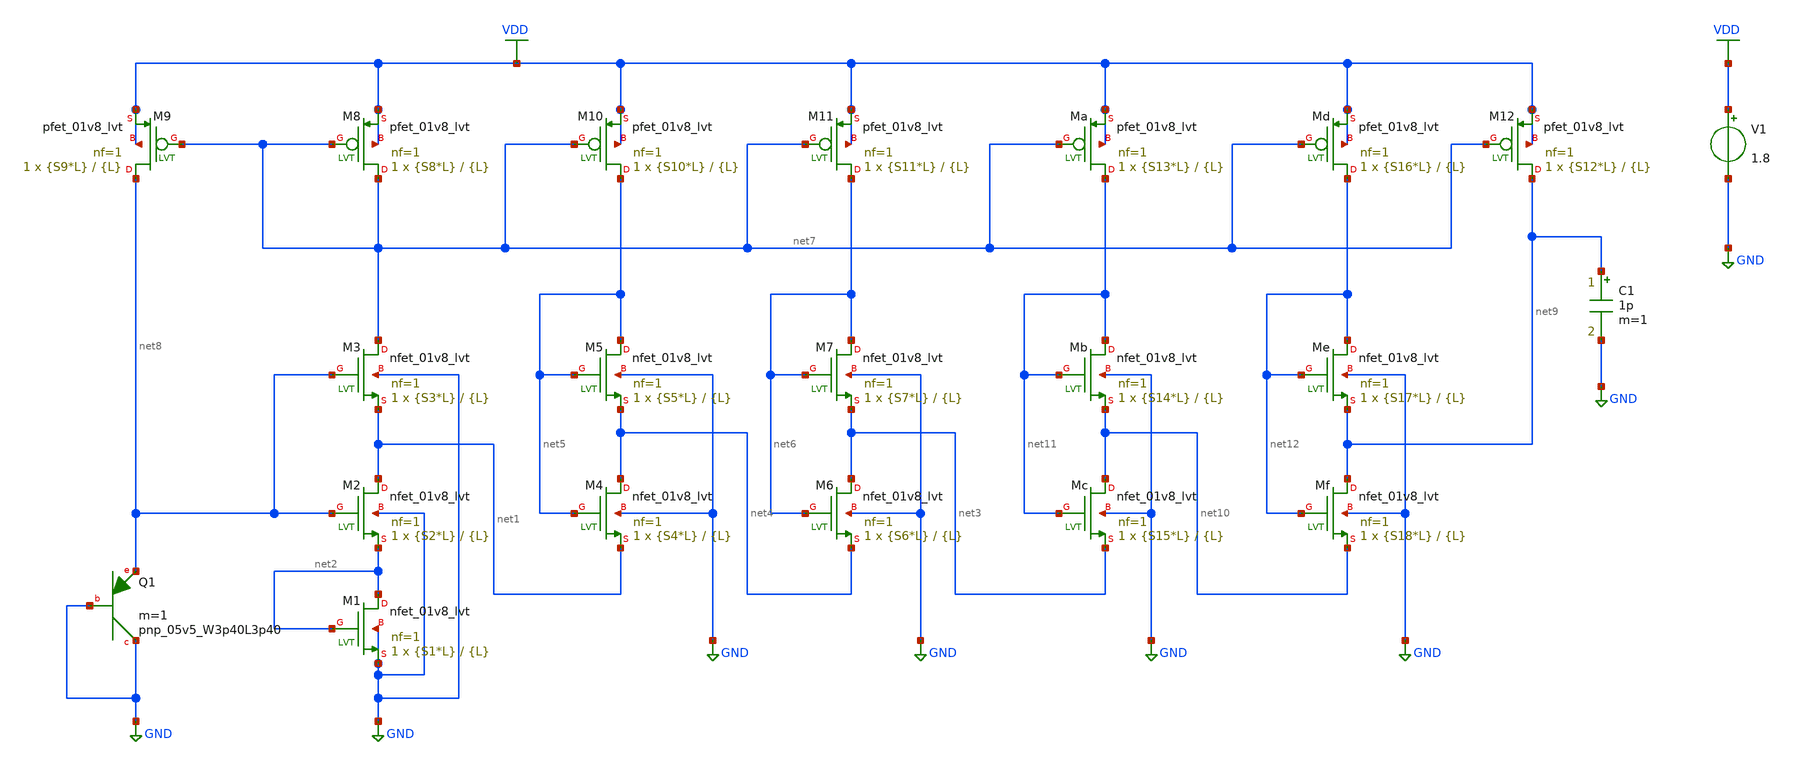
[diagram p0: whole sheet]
** sch_path: Design/Schematic/BGR_SKY130_v3.sch
**.subckt BGR_SKY130_v3
XM1 net2 net2 GND GND sky130_fd_pr__nfet_01v8_lvt L={L} W={S1*L} nf=1 ad='int((nf+1)/2) * W/nf * 0.29'
+ as='int((nf+2)/2) * W/nf * 0.29' pd='2*int((nf+1)/2) * (W/nf + 0.29)' ps='2*int((nf+2)/2) * (W/nf + 0.29)'
+ nrd='0.29 / W' nrs='0.29 / W' sa=0 sb=0 sd=0 mult=1 m=1
XM2 net1 net8 net2 GND sky130_fd_pr__nfet_01v8_lvt L={L} W={S2*L} nf=1 ad='int((nf+1)/2) * W/nf * 0.29'
+ as='int((nf+2)/2) * W/nf * 0.29' pd='2*int((nf+1)/2) * (W/nf + 0.29)' ps='2*int((nf+2)/2) * (W/nf + 0.29)'
+ nrd='0.29 / W' nrs='0.29 / W' sa=0 sb=0 sd=0 mult=1 m=1
XM3 net7 net8 net1 GND sky130_fd_pr__nfet_01v8_lvt L={L} W={S3*L} nf=1 ad='int((nf+1)/2) * W/nf * 0.29'
+ as='int((nf+2)/2) * W/nf * 0.29' pd='2*int((nf+1)/2) * (W/nf + 0.29)' ps='2*int((nf+2)/2) * (W/nf + 0.29)'
+ nrd='0.29 / W' nrs='0.29 / W' sa=0 sb=0 sd=0 mult=1 m=1
XM4 net4 net5 net1 GND sky130_fd_pr__nfet_01v8_lvt L={L} W={S4*L} nf=1 ad='int((nf+1)/2) * W/nf * 0.29'
+ as='int((nf+2)/2) * W/nf * 0.29' pd='2*int((nf+1)/2) * (W/nf + 0.29)' ps='2*int((nf+2)/2) * (W/nf + 0.29)'
+ nrd='0.29 / W' nrs='0.29 / W' sa=0 sb=0 sd=0 mult=1 m=1
XM5 net5 net5 net4 GND sky130_fd_pr__nfet_01v8_lvt L={L} W={S5*L} nf=1 ad='int((nf+1)/2) * W/nf * 0.29'
+ as='int((nf+2)/2) * W/nf * 0.29' pd='2*int((nf+1)/2) * (W/nf + 0.29)' ps='2*int((nf+2)/2) * (W/nf + 0.29)'
+ nrd='0.29 / W' nrs='0.29 / W' sa=0 sb=0 sd=0 mult=1 m=1
XM6 net3 net6 net4 GND sky130_fd_pr__nfet_01v8_lvt L={L} W={S6*L} nf=1 ad='int((nf+1)/2) * W/nf * 0.29'
+ as='int((nf+2)/2) * W/nf * 0.29' pd='2*int((nf+1)/2) * (W/nf + 0.29)' ps='2*int((nf+2)/2) * (W/nf + 0.29)'
+ nrd='0.29 / W' nrs='0.29 / W' sa=0 sb=0 sd=0 mult=1 m=1
XM7 net6 net6 net3 GND sky130_fd_pr__nfet_01v8_lvt L={L} W={S7*L} nf=1 ad='int((nf+1)/2) * W/nf * 0.29'
+ as='int((nf+2)/2) * W/nf * 0.29' pd='2*int((nf+1)/2) * (W/nf + 0.29)' ps='2*int((nf+2)/2) * (W/nf + 0.29)'
+ nrd='0.29 / W' nrs='0.29 / W' sa=0 sb=0 sd=0 mult=1 m=1
XM8 net7 net7 VDD VDD sky130_fd_pr__pfet_01v8_lvt L={L} W={S8*L} nf=1 ad='int((nf+1)/2) * W/nf * 0.29'
+ as='int((nf+2)/2) * W/nf * 0.29' pd='2*int((nf+1)/2) * (W/nf + 0.29)' ps='2*int((nf+2)/2) * (W/nf + 0.29)'
+ nrd='0.29 / W' nrs='0.29 / W' sa=0 sb=0 sd=0 mult=1 m=1
XM9 net8 net7 VDD VDD sky130_fd_pr__pfet_01v8_lvt L={L} W={S9*L} nf=1 ad='int((nf+1)/2) * W/nf * 0.29'
+ as='int((nf+2)/2) * W/nf * 0.29' pd='2*int((nf+1)/2) * (W/nf + 0.29)' ps='2*int((nf+2)/2) * (W/nf + 0.29)'
+ nrd='0.29 / W' nrs='0.29 / W' sa=0 sb=0 sd=0 mult=1 m=1
XM10 net5 net7 VDD VDD sky130_fd_pr__pfet_01v8_lvt L={L} W={S10*L} nf=1 ad='int((nf+1)/2) * W/nf * 0.29'
+ as='int((nf+2)/2) * W/nf * 0.29' pd='2*int((nf+1)/2) * (W/nf + 0.29)' ps='2*int((nf+2)/2) * (W/nf + 0.29)'
+ nrd='0.29 / W' nrs='0.29 / W' sa=0 sb=0 sd=0 mult=1 m=1
XM11 net6 net7 VDD VDD sky130_fd_pr__pfet_01v8_lvt L={L} W={S11*L} nf=1 ad='int((nf+1)/2) * W/nf * 0.29'
+ as='int((nf+2)/2) * W/nf * 0.29' pd='2*int((nf+1)/2) * (W/nf + 0.29)' ps='2*int((nf+2)/2) * (W/nf + 0.29)'
+ nrd='0.29 / W' nrs='0.29 / W' sa=0 sb=0 sd=0 mult=1 m=1
XM12 net9 net7 VDD VDD sky130_fd_pr__pfet_01v8_lvt L={L} W={S12*L} nf=1 ad='int((nf+1)/2) * W/nf * 0.29'
+ as='int((nf+2)/2) * W/nf * 0.29' pd='2*int((nf+1)/2) * (W/nf + 0.29)' ps='2*int((nf+2)/2) * (W/nf + 0.29)'
+ nrd='0.29 / W' nrs='0.29 / W' sa=0 sb=0 sd=0 mult=1 m=1
XMc net10 net11 net3 GND sky130_fd_pr__nfet_01v8_lvt L={L} W={S15*L} nf=1 ad='int((nf+1)/2) * W/nf * 0.29'
+ as='int((nf+2)/2) * W/nf * 0.29' pd='2*int((nf+1)/2) * (W/nf + 0.29)' ps='2*int((nf+2)/2) * (W/nf + 0.29)'
+ nrd='0.29 / W' nrs='0.29 / W' sa=0 sb=0 sd=0 mult=1 m=1
XMb net11 net11 net10 GND sky130_fd_pr__nfet_01v8_lvt L={L} W={S14*L} nf=1 ad='int((nf+1)/2) * W/nf * 0.29'
+ as='int((nf+2)/2) * W/nf * 0.29' pd='2*int((nf+1)/2) * (W/nf + 0.29)' ps='2*int((nf+2)/2) * (W/nf + 0.29)'
+ nrd='0.29 / W' nrs='0.29 / W' sa=0 sb=0 sd=0 mult=1 m=1
XMa net11 net7 VDD VDD sky130_fd_pr__pfet_01v8_lvt L={L} W={S13*L} nf=1 ad='int((nf+1)/2) * W/nf * 0.29'
+ as='int((nf+2)/2) * W/nf * 0.29' pd='2*int((nf+1)/2) * (W/nf + 0.29)' ps='2*int((nf+2)/2) * (W/nf + 0.29)'
+ nrd='0.29 / W' nrs='0.29 / W' sa=0 sb=0 sd=0 mult=1 m=1
XMf net9 net12 net10 GND sky130_fd_pr__nfet_01v8_lvt L={L} W={S18*L} nf=1 ad='int((nf+1)/2) * W/nf * 0.29'
+ as='int((nf+2)/2) * W/nf * 0.29' pd='2*int((nf+1)/2) * (W/nf + 0.29)' ps='2*int((nf+2)/2) * (W/nf + 0.29)'
+ nrd='0.29 / W' nrs='0.29 / W' sa=0 sb=0 sd=0 mult=1 m=1
XMe net12 net12 net9 GND sky130_fd_pr__nfet_01v8_lvt L={L} W={S17*L} nf=1 ad='int((nf+1)/2) * W/nf * 0.29'
+ as='int((nf+2)/2) * W/nf * 0.29' pd='2*int((nf+1)/2) * (W/nf + 0.29)' ps='2*int((nf+2)/2) * (W/nf + 0.29)'
+ nrd='0.29 / W' nrs='0.29 / W' sa=0 sb=0 sd=0 mult=1 m=1
XMd net12 net7 VDD VDD sky130_fd_pr__pfet_01v8_lvt L={L} W={S16*L} nf=1 ad='int((nf+1)/2) * W/nf * 0.29'
+ as='int((nf+2)/2) * W/nf * 0.29' pd='2*int((nf+1)/2) * (W/nf + 0.29)' ps='2*int((nf+2)/2) * (W/nf + 0.29)'
+ nrd='0.29 / W' nrs='0.29 / W' sa=0 sb=0 sd=0 mult=1 m=1
V1 VDD GND 1.8
C1 net9 GND 1p m=1
XQ1 GND GND net8 sky130_fd_pr__pnp_05v5_W3p40L3p40 m=1
**** begin user architecture code


** Analysis Requests **
.op
** Outputs Requests **
.control
run
show > opota.txt
.endc


 ** manual skywater pdks install (with patches applied)
*.lib $::SKYWATER_MODELS/sky130.lib.spice tt

** opencircuitdesign pdks install
.lib $::SKYWATER_MODELS/sky130.lib.spice tt

.param mc_mm_switch=0
.param mc_pr_switch=0

.include $::SKYWATER_MODELS/sky130_fd_pr__model__pnp.model.spice



** Analysis Requests **
** Outputs Requests **
.control
dc temp -40 125 5 V1 1.2 2.2 0.1
plot V(net2)
plot V(net8)

plot V(net9)
.endc




.param L = 1

*** 1st Branch: Controls amount of current in Bjt
.param S9 = 15

*** 2nd Branch:Controls Initial Offset
.param S8 = 1
.param S3 = 30
.param S2 = 30
.param S1 = 30

*** 3rd, 4th, 5th Branches: Fine Tuning slope for PTAT slope
.param S10 = 1
.param S5 = 5
.param S4 = 1

.param S11 = 1
.param S7 = 3
.param S6 = 1


.param S13 = 1
.param S14 = 5
.param S15 = 1

.param S16 = 1
.param S17 = 3
.param S18 = 1

*** Branch 6: Coarse Tuning for PTAT Slope
.param S12 = 1


**** end user architecture code
**.ends
.GLOBAL GND
.GLOBAL VDD
.end
